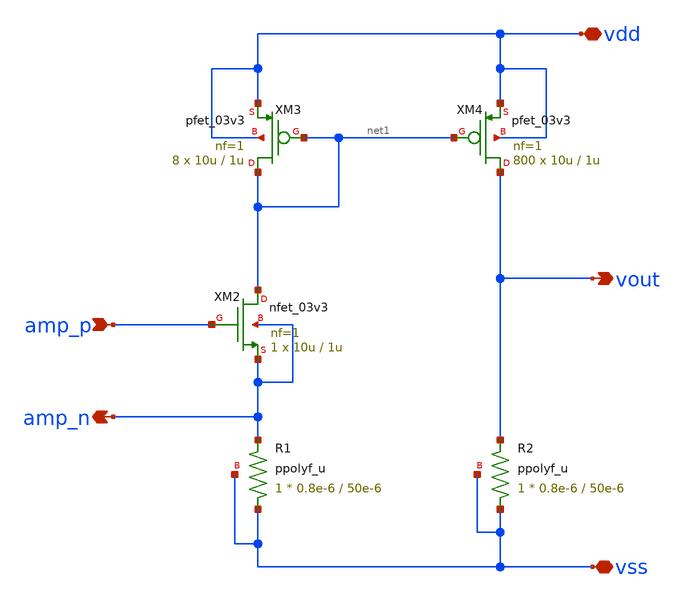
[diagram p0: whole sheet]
** sch_path: noritsuna/ldo/ldo_currentmirror.sch
**.subckt ldo_currentmirror vdd vss vout amp_p amp_n
*.iopin vdd
*.iopin vss
*.opin vout
*.ipin amp_p
*.opin amp_n
XM3 net1 net1 vdd vdd pfet_03v3 L=1u W=10u nf=1 ad='int((nf+1)/2) * W/nf * 0.18u' as='int((nf+2)/2) * W/nf * 0.18u'
+ pd='2*int((nf+1)/2) * (W/nf + 0.18u)' ps='2*int((nf+2)/2) * (W/nf + 0.18u)' nrd='0.18u / W' nrs='0.18u / W'
+ sa=0 sb=0 sd=0 m=8
XM4 vout net1 vdd vdd pfet_03v3 L=1u W=10u nf=1 ad='int((nf+1)/2) * W/nf * 0.18u' as='int((nf+2)/2) * W/nf * 0.18u'
+ pd='2*int((nf+1)/2) * (W/nf + 0.18u)' ps='2*int((nf+2)/2) * (W/nf + 0.18u)' nrd='0.18u / W' nrs='0.18u / W'
+ sa=0 sb=0 sd=0 m=800
XR1 vss amp_n vss ppolyf_u r_width=0.8e-6 r_length=50e-6 m=1
XM2 net1 amp_p amp_n amp_n nfet_03v3 L=1u W=10u nf=1 ad='int((nf+1)/2) * W/nf * 0.18u' as='int((nf+2)/2) * W/nf * 0.18u'
+ pd='2*int((nf+1)/2) * (W/nf + 0.18u)' ps='2*int((nf+2)/2) * (W/nf + 0.18u)' nrd='0.18u / W' nrs='0.18u / W'
+ sa=0 sb=0 sd=0 m=1
XR2 vss vout vss ppolyf_u r_width=0.8e-6 r_length=50e-6 m=1
**.ends
.end
